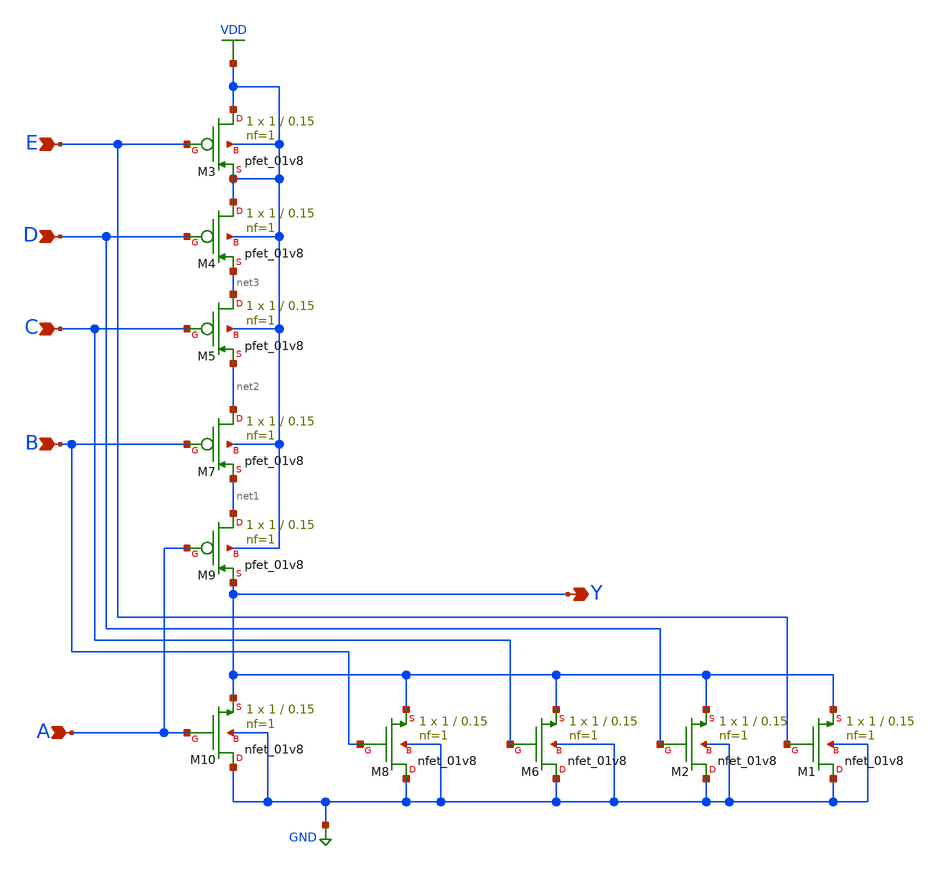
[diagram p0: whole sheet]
** sch_path: gates/NOR5.sch
**.subckt NOR5 A B Y C D E
*.ipin A
*.ipin B
*.opin Y
*.ipin C
*.ipin D
*.ipin E
XM1 GND E Y GND sky130_fd_pr__nfet_01v8 L=0.15 W=1 nf=1 ad='int((nf+1)/2) * W/nf * 0.29' as='int((nf+2)/2) * W/nf * 0.29'
+ pd='2*int((nf+1)/2) * (W/nf + 0.29)' ps='2*int((nf+2)/2) * (W/nf + 0.29)' nrd='0.29 / W' nrs='0.29 / W'
+ sa=0 sb=0 sd=0 mult=1 m=1
XM2 GND D Y GND sky130_fd_pr__nfet_01v8 L=0.15 W=1 nf=1 ad='int((nf+1)/2) * W/nf * 0.29' as='int((nf+2)/2) * W/nf * 0.29'
+ pd='2*int((nf+1)/2) * (W/nf + 0.29)' ps='2*int((nf+2)/2) * (W/nf + 0.29)' nrd='0.29 / W' nrs='0.29 / W'
+ sa=0 sb=0 sd=0 mult=1 m=1
XM3 VDD E VDD VDD sky130_fd_pr__pfet_01v8 L=0.15 W=1 nf=1 ad='int((nf+1)/2) * W/nf * 0.29' as='int((nf+2)/2) * W/nf * 0.29'
+ pd='2*int((nf+1)/2) * (W/nf + 0.29)' ps='2*int((nf+2)/2) * (W/nf + 0.29)' nrd='0.29 / W' nrs='0.29 / W'
+ sa=0 sb=0 sd=0 mult=1 m=1
XM4 VDD D net3 VDD sky130_fd_pr__pfet_01v8 L=0.15 W=1 nf=1 ad='int((nf+1)/2) * W/nf * 0.29' as='int((nf+2)/2) * W/nf * 0.29'
+ pd='2*int((nf+1)/2) * (W/nf + 0.29)' ps='2*int((nf+2)/2) * (W/nf + 0.29)' nrd='0.29 / W' nrs='0.29 / W'
+ sa=0 sb=0 sd=0 mult=1 m=1
XM5 net3 C net2 VDD sky130_fd_pr__pfet_01v8 L=0.15 W=1 nf=1 ad='int((nf+1)/2) * W/nf * 0.29' as='int((nf+2)/2) * W/nf * 0.29'
+ pd='2*int((nf+1)/2) * (W/nf + 0.29)' ps='2*int((nf+2)/2) * (W/nf + 0.29)' nrd='0.29 / W' nrs='0.29 / W'
+ sa=0 sb=0 sd=0 mult=1 m=1
XM6 GND C Y GND sky130_fd_pr__nfet_01v8 L=0.15 W=1 nf=1 ad='int((nf+1)/2) * W/nf * 0.29' as='int((nf+2)/2) * W/nf * 0.29'
+ pd='2*int((nf+1)/2) * (W/nf + 0.29)' ps='2*int((nf+2)/2) * (W/nf + 0.29)' nrd='0.29 / W' nrs='0.29 / W'
+ sa=0 sb=0 sd=0 mult=1 m=1
XM7 net2 B net1 VDD sky130_fd_pr__pfet_01v8 L=0.15 W=1 nf=1 ad='int((nf+1)/2) * W/nf * 0.29' as='int((nf+2)/2) * W/nf * 0.29'
+ pd='2*int((nf+1)/2) * (W/nf + 0.29)' ps='2*int((nf+2)/2) * (W/nf + 0.29)' nrd='0.29 / W' nrs='0.29 / W'
+ sa=0 sb=0 sd=0 mult=1 m=1
XM8 GND B Y GND sky130_fd_pr__nfet_01v8 L=0.15 W=1 nf=1 ad='int((nf+1)/2) * W/nf * 0.29' as='int((nf+2)/2) * W/nf * 0.29'
+ pd='2*int((nf+1)/2) * (W/nf + 0.29)' ps='2*int((nf+2)/2) * (W/nf + 0.29)' nrd='0.29 / W' nrs='0.29 / W'
+ sa=0 sb=0 sd=0 mult=1 m=1
XM9 net1 A Y VDD sky130_fd_pr__pfet_01v8 L=0.15 W=1 nf=1 ad='int((nf+1)/2) * W/nf * 0.29' as='int((nf+2)/2) * W/nf * 0.29'
+ pd='2*int((nf+1)/2) * (W/nf + 0.29)' ps='2*int((nf+2)/2) * (W/nf + 0.29)' nrd='0.29 / W' nrs='0.29 / W'
+ sa=0 sb=0 sd=0 mult=1 m=1
XM10 GND A Y GND sky130_fd_pr__nfet_01v8 L=0.15 W=1 nf=1 ad='int((nf+1)/2) * W/nf * 0.29' as='int((nf+2)/2) * W/nf * 0.29'
+ pd='2*int((nf+1)/2) * (W/nf + 0.29)' ps='2*int((nf+2)/2) * (W/nf + 0.29)' nrd='0.29 / W' nrs='0.29 / W'
+ sa=0 sb=0 sd=0 mult=1 m=1
**.ends
.GLOBAL VDD
.GLOBAL GND
.end
